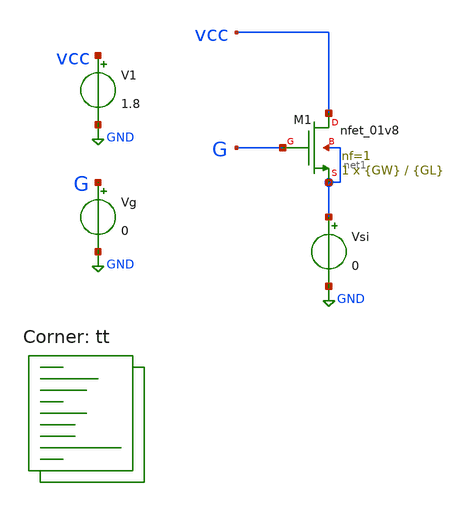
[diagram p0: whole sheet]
** sch_path: xschem/02-nfet-sweep2.sch
**.subckt 02-nfet-sweep2
XM1 vcc G net1 net1 sky130_fd_pr__nfet_01v8 L={GL} W={GW} nf=1 ad='int((nf+1)/2) * W/nf * 0.29' as='int((nf+2)/2) * W/nf * 0.29'
+ pd='2*int((nf+1)/2) * (W/nf + 0.29)' ps='2*int((nf+2)/2) * (W/nf + 0.29)' nrd='0.29 / W' nrs='0.29 / W'
+ sa=0 sb=0 sd=0 mult=1 m=1
V1 vcc GND 1.8
Vg G GND 0
Vsi net1 GND 0
**** begin user architecture code



.DC Vg 0 1.8 0.01

.param GW     = 0.5
.param GL     = 0.15

.options savecurrents
.control

  let gwstart = 0.5
  let gwstep  = 0.05
  let gwi     = gwstart

  repeat 10
    set gwvar=$&gwi
    echo Gate width = $gwvar
    alterparam GW = $gwvar
    save all
    run
    write 02.raw G i(vsi)
    set appendwrite
    reset
    let gwi = gwi + gwstep
  end

.endc



.lib $::SKYWATER_MODELS/sky130.lib.spice tt
**** end user architecture code
**.ends
.GLOBAL GND
.end
